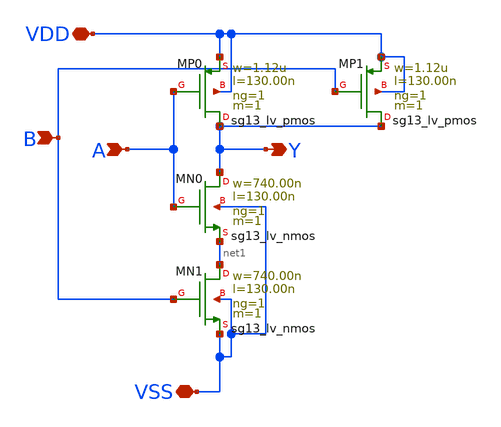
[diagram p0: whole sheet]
** sch_path: xschem/NAND.sch
**.subckt NAND Y A VDD VSS B
*.opin Y
*.ipin A
*.iopin VDD
*.iopin VSS
*.ipin B
XMN0 Y A net1 VSS sg13_lv_nmos w=740.00n l=130.00n ng=1 m=1 mm_ok=1
XMP0 Y A VDD VDD sg13_lv_pmos w=1.12u l=130.00n ng=1 m=1 mm_ok=1
XMP1 Y B VDD VDD sg13_lv_pmos w=1.12u l=130.00n ng=1 m=1 mm_ok=1
XMN1 net1 B VSS VSS sg13_lv_nmos w=740.00n l=130.00n ng=1 m=1 mm_ok=1
**.ends
.end
